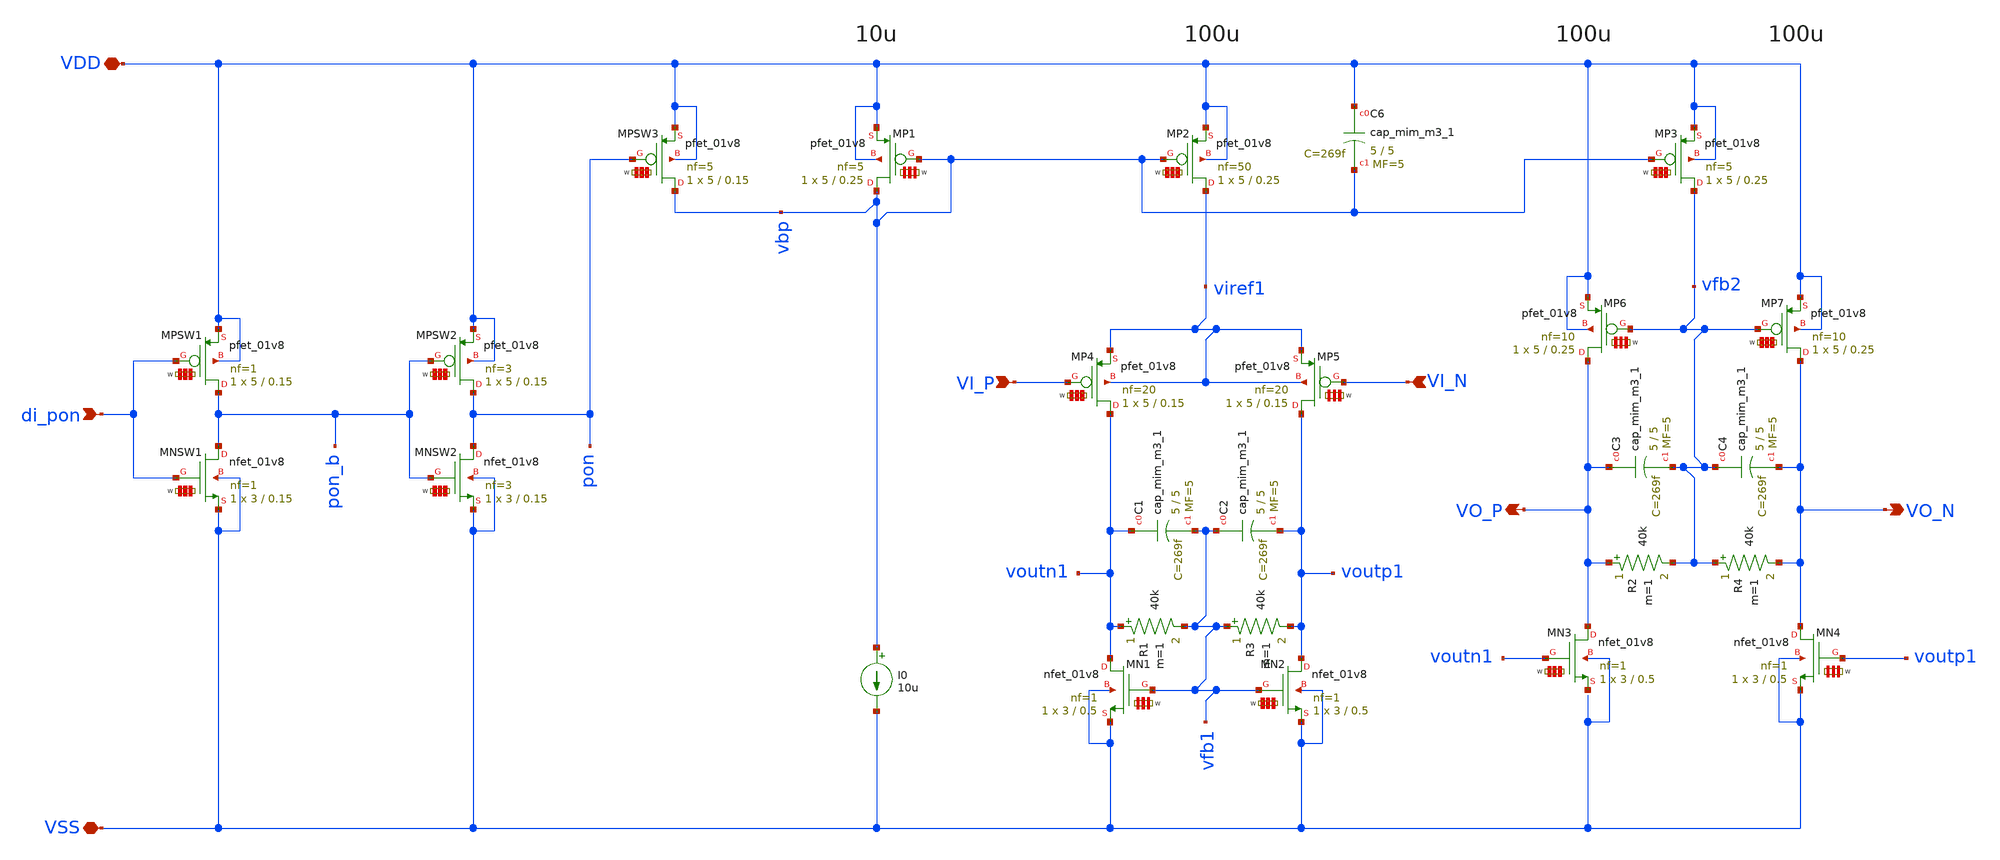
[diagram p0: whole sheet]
** sch_path: xschem/amp.sch
**.subckt amp VSS VDD VI_P di_pon VI_N VO_N VO_P
*.iopin VSS
*.iopin VDD
*.ipin VI_P
*.ipin di_pon
*.ipin VI_N
*.opin VO_N
*.opin VO_P
XMP1 vbp vbp VDD VDD sky130_fd_pr__pfet_01v8 L=0.25 W='5 * 5 ' nf=5 ad='int((nf+1)/2) * W / nf * 0.29'
+ as='int((nf+2)/2) * W / nf * 0.29' pd='2*int((nf+1)/2) * (W / nf + 0.29)' ps='2*int((nf+2)/2) * (W / nf + 0.29)'
+ nrd='0.29 / W ' nrs='0.29 / W ' sa=0 sb=0 sd=0 mult=1 m=1
XMPSW3 vbp pon VDD VDD sky130_fd_pr__pfet_01v8 L=0.15 W='5 * 5 ' nf=5 ad='int((nf+1)/2) * W / nf * 0.29'
+ as='int((nf+2)/2) * W / nf * 0.29' pd='2*int((nf+1)/2) * (W / nf + 0.29)' ps='2*int((nf+2)/2) * (W / nf + 0.29)'
+ nrd='0.29 / W ' nrs='0.29 / W ' sa=0 sb=0 sd=0 mult=1 m=1
XMNSW1 pon_b di_pon VSS VSS sky130_fd_pr__nfet_01v8 L=0.15 W='3 * 1 ' nf=1 ad='int((nf+1)/2) * W / nf * 0.29'
+ as='int((nf+2)/2) * W / nf * 0.29' pd='2*int((nf+1)/2) * (W / nf + 0.29)' ps='2*int((nf+2)/2) * (W / nf + 0.29)'
+ nrd='0.29 / W ' nrs='0.29 / W ' sa=0 sb=0 sd=0 mult=1 m=1
XMPSW1 pon_b di_pon VDD VDD sky130_fd_pr__pfet_01v8 L=0.15 W='5 * 1 ' nf=1 ad='int((nf+1)/2) * W / nf * 0.29'
+ as='int((nf+2)/2) * W / nf * 0.29' pd='2*int((nf+1)/2) * (W / nf + 0.29)' ps='2*int((nf+2)/2) * (W / nf + 0.29)'
+ nrd='0.29 / W ' nrs='0.29 / W ' sa=0 sb=0 sd=0 mult=1 m=1
XMNSW2 pon pon_b VSS VSS sky130_fd_pr__nfet_01v8 L=0.15 W='3 * 3 ' nf=3 ad='int((nf+1)/2) * W / nf * 0.29'
+ as='int((nf+2)/2) * W / nf * 0.29' pd='2*int((nf+1)/2) * (W / nf + 0.29)' ps='2*int((nf+2)/2) * (W / nf + 0.29)'
+ nrd='0.29 / W ' nrs='0.29 / W ' sa=0 sb=0 sd=0 mult=1 m=1
XMPSW2 pon pon_b VDD VDD sky130_fd_pr__pfet_01v8 L=0.15 W='5 * 3 ' nf=3 ad='int((nf+1)/2) * W / nf * 0.29'
+ as='int((nf+2)/2) * W / nf * 0.29' pd='2*int((nf+1)/2) * (W / nf + 0.29)' ps='2*int((nf+2)/2) * (W / nf + 0.29)'
+ nrd='0.29 / W ' nrs='0.29 / W ' sa=0 sb=0 sd=0 mult=1 m=1
XMP2 viref1 vbp VDD VDD sky130_fd_pr__pfet_01v8 L=0.25 W='5 * 50 ' nf=50 ad='int((nf+1)/2) * W / nf * 0.29'
+ as='int((nf+2)/2) * W / nf * 0.29' pd='2*int((nf+1)/2) * (W / nf + 0.29)' ps='2*int((nf+2)/2) * (W / nf + 0.29)'
+ nrd='0.29 / W ' nrs='0.29 / W ' sa=0 sb=0 sd=0 mult=1 m=1
XMP3 vfb2 vbp VDD VDD sky130_fd_pr__pfet_01v8 L=0.25 W='5 * 5 ' nf=5 ad='int((nf+1)/2) * W / nf * 0.29'
+ as='int((nf+2)/2) * W / nf * 0.29' pd='2*int((nf+1)/2) * (W / nf + 0.29)' ps='2*int((nf+2)/2) * (W / nf + 0.29)'
+ nrd='0.29 / W ' nrs='0.29 / W ' sa=0 sb=0 sd=0 mult=1 m=1
XC6 VDD vbp sky130_fd_pr__cap_mim_m3_1 W=5 L=5 MF=5 m=5
XMP4 voutn1 VI_P viref1 viref1 sky130_fd_pr__pfet_01v8 L=0.15 W='5 * 20 ' nf=20 ad='int((nf+1)/2) * W / nf * 0.29'
+ as='int((nf+2)/2) * W / nf * 0.29' pd='2*int((nf+1)/2) * (W / nf + 0.29)' ps='2*int((nf+2)/2) * (W / nf + 0.29)'
+ nrd='0.29 / W ' nrs='0.29 / W ' sa=0 sb=0 sd=0 mult=1 m=1
XMP5 voutp1 VI_N viref1 viref1 sky130_fd_pr__pfet_01v8 L=0.15 W='5 * 20 ' nf=20 ad='int((nf+1)/2) * W / nf * 0.29'
+ as='int((nf+2)/2) * W / nf * 0.29' pd='2*int((nf+1)/2) * (W / nf + 0.29)' ps='2*int((nf+2)/2) * (W / nf + 0.29)'
+ nrd='0.29 / W ' nrs='0.29 / W ' sa=0 sb=0 sd=0 mult=1 m=1
XMN1 voutn1 vfb1 VSS VSS sky130_fd_pr__nfet_01v8 L=0.5 W='3 * 1 ' nf=1 ad='int((nf+1)/2) * W / nf * 0.29'
+ as='int((nf+2)/2) * W / nf * 0.29' pd='2*int((nf+1)/2) * (W / nf + 0.29)' ps='2*int((nf+2)/2) * (W / nf + 0.29)'
+ nrd='0.29 / W ' nrs='0.29 / W ' sa=0 sb=0 sd=0 mult=1 m=1
XMN2 voutp1 vfb1 VSS VSS sky130_fd_pr__nfet_01v8 L=0.5 W='3 * 1 ' nf=1 ad='int((nf+1)/2) * W / nf * 0.29'
+ as='int((nf+2)/2) * W / nf * 0.29' pd='2*int((nf+1)/2) * (W / nf + 0.29)' ps='2*int((nf+2)/2) * (W / nf + 0.29)'
+ nrd='0.29 / W ' nrs='0.29 / W ' sa=0 sb=0 sd=0 mult=1 m=1
R1 voutn1 vfb1 40k m=1
R3 vfb1 voutp1 40k m=1
XMN3 VO_P voutn1 net1 VSS sky130_fd_pr__nfet_01v8 L=0.5 W='3 * 1 ' nf=1 ad='int((nf+1)/2) * W / nf * 0.29'
+ as='int((nf+2)/2) * W / nf * 0.29' pd='2*int((nf+1)/2) * (W / nf + 0.29)' ps='2*int((nf+2)/2) * (W / nf + 0.29)'
+ nrd='0.29 / W ' nrs='0.29 / W ' sa=0 sb=0 sd=0 mult=1 m=1
XMN4 VO_N voutp1 VSS VSS sky130_fd_pr__nfet_01v8 L=0.5 W='3 * 1 ' nf=1 ad='int((nf+1)/2) * W / nf * 0.29'
+ as='int((nf+2)/2) * W / nf * 0.29' pd='2*int((nf+1)/2) * (W / nf + 0.29)' ps='2*int((nf+2)/2) * (W / nf + 0.29)'
+ nrd='0.29 / W ' nrs='0.29 / W ' sa=0 sb=0 sd=0 mult=1 m=1
XMP6 VO_P vfb2 VDD VDD sky130_fd_pr__pfet_01v8 L=0.25 W='5 * 10 ' nf=10 ad='int((nf+1)/2) * W / nf * 0.29'
+ as='int((nf+2)/2) * W / nf * 0.29' pd='2*int((nf+1)/2) * (W / nf + 0.29)' ps='2*int((nf+2)/2) * (W / nf + 0.29)'
+ nrd='0.29 / W ' nrs='0.29 / W ' sa=0 sb=0 sd=0 mult=1 m=1
XMP7 VO_N vfb2 VDD VDD sky130_fd_pr__pfet_01v8 L=0.25 W='5 * 10 ' nf=10 ad='int((nf+1)/2) * W / nf * 0.29'
+ as='int((nf+2)/2) * W / nf * 0.29' pd='2*int((nf+1)/2) * (W / nf + 0.29)' ps='2*int((nf+2)/2) * (W / nf + 0.29)'
+ nrd='0.29 / W ' nrs='0.29 / W ' sa=0 sb=0 sd=0 mult=1 m=1
XC1 voutn1 vfb1 sky130_fd_pr__cap_mim_m3_1 W=5 L=5 MF=5 m=5
XC2 vfb1 voutp1 sky130_fd_pr__cap_mim_m3_1 W=5 L=5 MF=5 m=5
I0 vbp VSS 10u
R2 VO_P vfb2 40k m=1
R4 vfb2 VO_N 40k m=1
XC3 VO_P vfb2 sky130_fd_pr__cap_mim_m3_1 W=5 L=5 MF=5 m=5
XC4 vfb2 VO_N sky130_fd_pr__cap_mim_m3_1 W=5 L=5 MF=5 m=5
**.ends
.end
